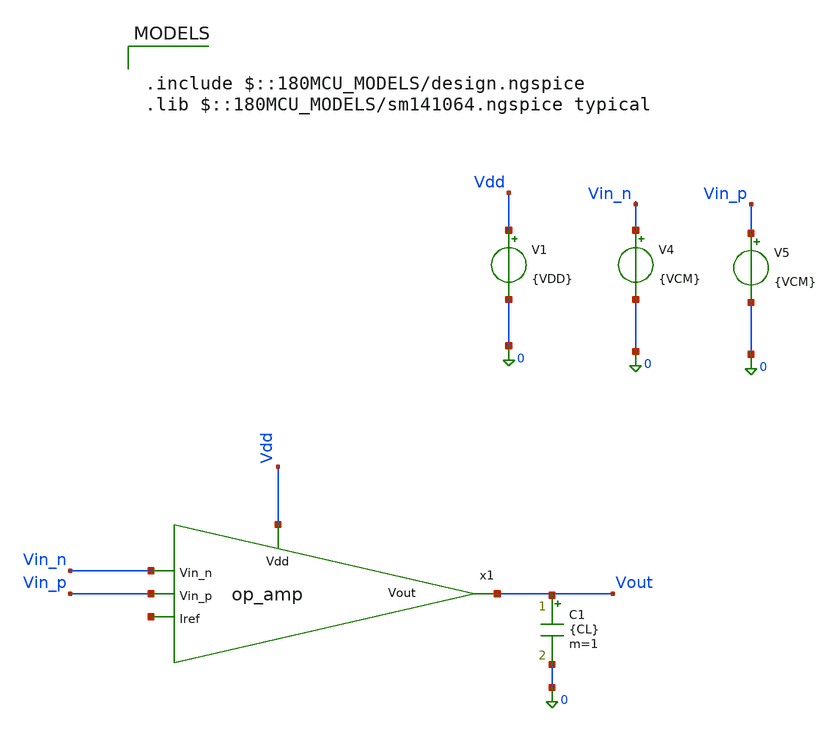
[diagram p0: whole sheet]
** sch_path: blocks/adc/lvds/ota_test.sch
**.subckt ota_test
C1 net1 0 {CL} m=1
V1 Vdd 0 {VDD}
V4 Vin_n 0 {VCM}
V5 Vin_p 0 {VCM}
x1 Vdd Vout Vin_n Vin_p net2 op_amp
**** begin user architecture code


.param VDD=3.3
.param VCM=1.2
.param VB1=0
.param VB2=0
.param CL=10f

.control
* ============================================================
* Output file
* ============================================================
let vb1_start = 0
let vb1_step  = 0.1
let vb1_n     = 33

let vb2_start = 0
let vb2_step  = 0.1
let vb2_n     = 33


shell rm /foss/designs/trans_testing/ota_testing/ota_bias_op_loop.txt

set appendwrite
set wr_singlescale

* ============================================================
* Main VB1 / VB2 operating-point loop
* ============================================================


  let i = 0

  while i le vb1_n

    let vb1_val = vb1_start + i*vb1_step
    let j = 0

    echo Starting VB1 = $&vb1_val

    while j le vb2_n

      let vb2_val = vb2_start + j*vb2_step

      alter V2 = $&vb1_val
      alter V3 = $&vb2_val

      op

      let vb1_save = vb1_val
      let vb2_save = vb2_val
      let vout_save = v(vout)

      let xm1_type  = 1
      let xm1_id    = @m.x1.xm1.m0[id]
      let xm1_vgs   = @m.x1.xm1.m0[vgs]
      let xm1_vds   = @m.x1.xm1.m0[vds]
      let xm1_vth   = @m.x1.xm1.m0[vth]
      let xm1_vdsat = @m.x1.xm1.m0[vdsat]
      let xm1_gm    = @m.x1.xm1.m0[gm]
      let xm1_gds   = @m.x1.xm1.m0[gds]

      let xm2_type  = 1
      let xm2_id    = @m.x1.xm2.m0[id]
      let xm2_vgs   = @m.x1.xm2.m0[vgs]
      let xm2_vds   = @m.x1.xm2.m0[vds]
      let xm2_vth   = @m.x1.xm2.m0[vth]
      let xm2_vdsat = @m.x1.xm2.m0[vdsat]
      let xm2_gm    = @m.x1.xm2.m0[gm]
      let xm2_gds   = @m.x1.xm2.m0[gds]

      let xm3_type  = 1
      let xm3_id    = @m.x1.xm3.m0[id]
      let xm3_vgs   = @m.x1.xm3.m0[vgs]
      let xm3_vds   = @m.x1.xm3.m0[vds]
      let xm3_vth   = @m.x1.xm3.m0[vth]
      let xm3_vdsat = @m.x1.xm3.m0[vdsat]
      let xm3_gm    = @m.x1.xm3.m0[gm]
      let xm3_gds   = @m.x1.xm3.m0[gds]

      let xm4_type  = 1
      let xm4_id    = @m.x1.xm4.m0[id]
      let xm4_vgs   = @m.x1.xm4.m0[vgs]
      let xm4_vds   = @m.x1.xm4.m0[vds]
      let xm4_vth   = @m.x1.xm4.m0[vth]
      let xm4_vdsat = @m.x1.xm4.m0[vdsat]
      let xm4_gm    = @m.x1.xm4.m0[gm]
      let xm4_gds   = @m.x1.xm4.m0[gds]

      let xm5_type  = 0
      let xm5_id    = @m.x1.xm5.m0[id]
      let xm5_vgs   = @m.x1.xm5.m0[vgs]
      let xm5_vds   = @m.x1.xm5.m0[vds]
      let xm5_vth   = @m.x1.xm5.m0[vth]
      let xm5_vdsat = @m.x1.xm5.m0[vdsat]
      let xm5_gm    = @m.x1.xm5.m0[gm]
      let xm5_gds   = @m.x1.xm5.m0[gds]

      let xm6_type  = 0
      let xm6_id    = @m.x1.xm6.m0[id]
      let xm6_vgs   = @m.x1.xm6.m0[vgs]
      let xm6_vds   = @m.x1.xm6.m0[vds]
      let xm6_vth   = @m.x1.xm6.m0[vth]
      let xm6_vdsat = @m.x1.xm6.m0[vdsat]
      let xm6_gm    = @m.x1.xm6.m0[gm]
      let xm6_gds   = @m.x1.xm6.m0[gds]

      let xm7_type  = 1
      let xm7_id    = @m.x1.xm7.m0[id]
      let xm7_vgs   = @m.x1.xm7.m0[vgs]
      let xm7_vds   = @m.x1.xm7.m0[vds]
      let xm7_vth   = @m.x1.xm7.m0[vth]
      let xm7_vdsat = @m.x1.xm7.m0[vdsat]
      let xm7_gm    = @m.x1.xm7.m0[gm]
      let xm7_gds   = @m.x1.xm7.m0[gds]

      let xm8_type  = 1
      let xm8_id    = @m.x1.xm8.m0[id]
      let xm8_vgs   = @m.x1.xm8.m0[vgs]
      let xm8_vds   = @m.x1.xm8.m0[vds]
      let xm8_vth   = @m.x1.xm8.m0[vth]
      let xm8_vdsat = @m.x1.xm8.m0[vdsat]
      let xm8_gm    = @m.x1.xm8.m0[gm]
      let xm8_gds   = @m.x1.xm8.m0[gds]

      let xm9_type  = 1
      let xm9_id    = @m.x1.xm9.m0[id]
      let xm9_vgs   = @m.x1.xm9.m0[vgs]
      let xm9_vds   = @m.x1.xm9.m0[vds]
      let xm9_vth   = @m.x1.xm9.m0[vth]
      let xm9_vdsat = @m.x1.xm9.m0[vdsat]
      let xm9_gm    = @m.x1.xm9.m0[gm]
      let xm9_gds   = @m.x1.xm9.m0[gds]

      let xm10_type  = 1
      let xm10_id    = @m.x1.xm10.m0[id]
      let xm10_vgs   = @m.x1.xm10.m0[vgs]
      let xm10_vds   = @m.x1.xm10.m0[vds]
      let xm10_vth   = @m.x1.xm10.m0[vth]
      let xm10_vdsat = @m.x1.xm10.m0[vdsat]
      let xm10_gm    = @m.x1.xm10.m0[gm]
      let xm10_gds   = @m.x1.xm10.m0[gds]

      let xm11_type  = 0
      let xm11_id    = @m.x1.xm11.m0[id]
      let xm11_vgs   = @m.x1.xm11.m0[vgs]
      let xm11_vds   = @m.x1.xm11.m0[vds]
      let xm11_vth   = @m.x1.xm11.m0[vth]
      let xm11_vdsat = @m.x1.xm11.m0[vdsat]
      let xm11_gm    = @m.x1.xm11.m0[gm]
      let xm11_gds   = @m.x1.xm11.m0[gds]

      let xm12_type  = 0
      let xm12_id    = @m.x1.xm12.m0[id]
      let xm12_vgs   = @m.x1.xm12.m0[vgs]
      let xm12_vds   = @m.x1.xm12.m0[vds]
      let xm12_vth   = @m.x1.xm12.m0[vth]
      let xm12_vdsat = @m.x1.xm12.m0[vdsat]
      let xm12_gm    = @m.x1.xm12.m0[gm]
      let xm12_gds   = @m.x1.xm12.m0[gds]

      let xm13_type  = 0
      let xm13_id    = @m.x1.xm13.m0[id]
      let xm13_vgs   = @m.x1.xm13.m0[vgs]
      let xm13_vds   = @m.x1.xm13.m0[vds]
      let xm13_vth   = @m.x1.xm13.m0[vth]
      let xm13_vdsat = @m.x1.xm13.m0[vdsat]
      let xm13_gm    = @m.x1.xm13.m0[gm]
      let xm13_gds   = @m.x1.xm13.m0[gds]

      let xm14_type  = 0
      let xm14_id    = @m.x1.xm14.m0[id]
      let xm14_vgs   = @m.x1.xm14.m0[vgs]
      let xm14_vds   = @m.x1.xm14.m0[vds]
      let xm14_vth   = @m.x1.xm14.m0[vth]
      let xm14_vdsat = @m.x1.xm14.m0[vdsat]
      let xm14_gm    = @m.x1.xm14.m0[gm]
      let xm14_gds   = @m.x1.xm14.m0[gds]

	wrdata /foss/designs/trans_testing/ota_testing/ota_bias_op_loop.txt vb1_save vb2_save vout_save
+ xm1_type xm1_id xm1_vgs xm1_vds xm1_vth xm1_vdsat xm1_gm xm1_gds xm2_type xm2_id xm2_vgs xm2_vds xm2_vth
+ xm2_vdsat xm2_gm xm2_gds xm3_type xm3_id xm3_vgs xm3_vds xm3_vth xm3_vdsat xm3_gm xm3_gds xm4_type xm4_id
+ xm4_vgs xm4_vds xm4_vth xm4_vdsat xm4_gm xm4_gds xm5_type xm5_id xm5_vgs xm5_vds xm5_vth xm5_vdsat xm5_gm
+ xm5_gds xm6_type xm6_id xm6_vgs xm6_vds xm6_vth xm6_vdsat xm6_gm xm6_gds xm7_type xm7_id xm7_vgs xm7_vds
+ xm7_vth xm7_vdsat xm7_gm xm7_gds xm8_type xm8_id xm8_vgs xm8_vds xm8_vth xm8_vdsat xm8_gm xm8_gds xm9_type
+ xm9_id xm9_vgs xm9_vds xm9_vth xm9_vdsat xm9_gm xm9_gds xm10_type xm10_id xm10_vgs xm10_vds xm10_vth
+ xm10_vdsat xm10_gm xm10_gds xm11_type xm11_id xm11_vgs xm11_vds xm11_vth xm11_vdsat xm11_gm xm11_gds xm12_type
+ xm12_id xm12_vgs xm12_vds xm12_vth xm12_vdsat xm12_gm xm12_gds xm13_type xm13_id xm13_vgs xm13_vds xm13_vth
+ xm13_vdsat xm13_gm xm13_gds xm14_type xm14_id xm14_vgs xm14_vds xm14_vth xm14_vdsat xm14_gm xm14_gds
      let j = j + 1

    end

    let i = i + 1

  end


.endc



.include $::180MCU_MODELS/design.ngspice
.lib $::180MCU_MODELS/sm141064.ngspice typical

**** end user architecture code
**.ends

* expanding   symbol:  op_amp.sym # of pins=5
** sym_path: blocks/adc/lvds/op_amp.sym
** sch_path: blocks/adc/lvds/op_amp.sch
.subckt op_amp Vdd Vout Vin_n Vin_p Iref
*.ipin Vdd
*.ipin Vin_p
*.ipin Vin_n
*.opin Vout
*.ipin Iref
XM1 net2 net3 Vdd Vdd pfet_03v3 L=0.28u W=10.5u nf=1 ad='int((nf+1)/2) * W/nf * 0.18u' as='int((nf+2)/2) * W/nf * 0.18u'
+ pd='2*int((nf+1)/2) * (W/nf + 0.18u)' ps='2*int((nf+2)/2) * (W/nf + 0.18u)' nrd='0.18u / W' nrs='0.18u / W'
+ sa=0 sb=0 sd=0 m=1
XM2 net1 net4 Vdd Vdd pfet_03v3 L=0.28u W=10.5u nf=1 ad='int((nf+1)/2) * W/nf * 0.18u' as='int((nf+2)/2) * W/nf * 0.18u'
+ pd='2*int((nf+1)/2) * (W/nf + 0.18u)' ps='2*int((nf+2)/2) * (W/nf + 0.18u)' nrd='0.18u / W' nrs='0.18u / W'
+ sa=0 sb=0 sd=0 m=1
XM3 net3 Vb2 net2 Vdd pfet_03v3 L=0.28u W=10.5u nf=1 ad='int((nf+1)/2) * W/nf * 0.18u' as='int((nf+2)/2) * W/nf * 0.18u'
+ pd='2*int((nf+1)/2) * (W/nf + 0.18u)' ps='2*int((nf+2)/2) * (W/nf + 0.18u)' nrd='0.18u / W' nrs='0.18u / W'
+ sa=0 sb=0 sd=0 m=1
XM4 net4 Vb2 net1 Vdd pfet_03v3 L=0.28u W=10.5u nf=1 ad='int((nf+1)/2) * W/nf * 0.18u' as='int((nf+2)/2) * W/nf * 0.18u'
+ pd='2*int((nf+1)/2) * (W/nf + 0.18u)' ps='2*int((nf+2)/2) * (W/nf + 0.18u)' nrd='0.18u / W' nrs='0.18u / W'
+ sa=0 sb=0 sd=0 m=1
XM5 net4 Vin_p net5 0 nfet_03v3 L=0.28u W=52.5u nf=15 ad='int((nf+1)/2) * W/nf * 0.18u' as='int((nf+2)/2) * W/nf * 0.18u'
+ pd='2*int((nf+1)/2) * (W/nf + 0.18u)' ps='2*int((nf+2)/2) * (W/nf + 0.18u)' nrd='0.18u / W' nrs='0.18u / W'
+ sa=0 sb=0 sd=0 m=1
XM6 net3 Vin_n net5 0 nfet_03v3 L=0.28u W=52.5u nf=15 ad='int((nf+1)/2) * W/nf * 0.18u' as='int((nf+2)/2) * W/nf * 0.18u'
+ pd='2*int((nf+1)/2) * (W/nf + 0.18u)' ps='2*int((nf+2)/2) * (W/nf + 0.18u)' nrd='0.18u / W' nrs='0.18u / W'
+ sa=0 sb=0 sd=0 m=1
XM7 net6 net4 Vdd Vdd pfet_03v3 L=0.28u W=10.5u nf=1 ad='int((nf+1)/2) * W/nf * 0.18u' as='int((nf+2)/2) * W/nf * 0.18u'
+ pd='2*int((nf+1)/2) * (W/nf + 0.18u)' ps='2*int((nf+2)/2) * (W/nf + 0.18u)' nrd='0.18u / W' nrs='0.18u / W'
+ sa=0 sb=0 sd=0 m=1
XM9 net7 net3 Vdd Vdd pfet_03v3 L=0.28u W=10.5u nf=1 ad='int((nf+1)/2) * W/nf * 0.18u' as='int((nf+2)/2) * W/nf * 0.18u'
+ pd='2*int((nf+1)/2) * (W/nf + 0.18u)' ps='2*int((nf+2)/2) * (W/nf + 0.18u)' nrd='0.18u / W' nrs='0.18u / W'
+ sa=0 sb=0 sd=0 m=1
XM11 net8 Vb2 net10 0 nfet_03v3 L=0.28u W=5.25u nf=1 ad='int((nf+1)/2) * W/nf * 0.18u' as='int((nf+2)/2) * W/nf * 0.18u'
+ pd='2*int((nf+1)/2) * (W/nf + 0.18u)' ps='2*int((nf+2)/2) * (W/nf + 0.18u)' nrd='0.18u / W' nrs='0.18u / W'
+ sa=0 sb=0 sd=0 m=1
XM12 Vout Vb2 net9 0 nfet_03v3 L=0.28u W=5.25u nf=1 ad='int((nf+1)/2) * W/nf * 0.18u' as='int((nf+2)/2) * W/nf * 0.18u'
+ pd='2*int((nf+1)/2) * (W/nf + 0.18u)' ps='2*int((nf+2)/2) * (W/nf + 0.18u)' nrd='0.18u / W' nrs='0.18u / W'
+ sa=0 sb=0 sd=0 m=1
XM13 net10 net8 0 0 nfet_03v3 L=0.28u W=5.25u nf=1 ad='int((nf+1)/2) * W/nf * 0.18u' as='int((nf+2)/2) * W/nf * 0.18u'
+ pd='2*int((nf+1)/2) * (W/nf + 0.18u)' ps='2*int((nf+2)/2) * (W/nf + 0.18u)' nrd='0.18u / W' nrs='0.18u / W'
+ sa=0 sb=0 sd=0 m=1
XM14 net9 net8 0 0 nfet_03v3 L=0.28u W=5.25u nf=1 ad='int((nf+1)/2) * W/nf * 0.18u' as='int((nf+2)/2) * W/nf * 0.18u'
+ pd='2*int((nf+1)/2) * (W/nf + 0.18u)' ps='2*int((nf+2)/2) * (W/nf + 0.18u)' nrd='0.18u / W' nrs='0.18u / W'
+ sa=0 sb=0 sd=0 m=1
XM8 net8 0 net6 Vdd pfet_03v3 L=0.28u W=10.5u nf=1 ad='int((nf+1)/2) * W/nf * 0.18u' as='int((nf+2)/2) * W/nf * 0.18u'
+ pd='2*int((nf+1)/2) * (W/nf + 0.18u)' ps='2*int((nf+2)/2) * (W/nf + 0.18u)' nrd='0.18u / W' nrs='0.18u / W'
+ sa=0 sb=0 sd=0 m=1
XM10 Vout 0 net7 Vdd pfet_03v3 L=0.28u W=10.5u nf=1 ad='int((nf+1)/2) * W/nf * 0.18u' as='int((nf+2)/2) * W/nf * 0.18u'
+ pd='2*int((nf+1)/2) * (W/nf + 0.18u)' ps='2*int((nf+2)/2) * (W/nf + 0.18u)' nrd='0.18u / W' nrs='0.18u / W'
+ sa=0 sb=0 sd=0 m=1
XM15 net5 net11 0 0 nfet_03v3 L=1u W=80u nf=20 ad='int((nf+1)/2) * W/nf * 0.18u' as='int((nf+2)/2) * W/nf * 0.18u'
+ pd='2*int((nf+1)/2) * (W/nf + 0.18u)' ps='2*int((nf+2)/2) * (W/nf + 0.18u)' nrd='0.18u / W' nrs='0.18u / W'
+ sa=0 sb=0 sd=0 m=1
XM16 Iref Iref Vdd Vdd pfet_03v3 L=1u W=20u nf=1 ad='int((nf+1)/2) * W/nf * 0.18u' as='int((nf+2)/2) * W/nf * 0.18u'
+ pd='2*int((nf+1)/2) * (W/nf + 0.18u)' ps='2*int((nf+2)/2) * (W/nf + 0.18u)' nrd='0.18u / W' nrs='0.18u / W'
+ sa=0 sb=0 sd=0 m=1
XM17 net11 Iref Vdd Vdd pfet_03v3 L=1u W=80u nf=1 ad='int((nf+1)/2) * W/nf * 0.18u' as='int((nf+2)/2) * W/nf * 0.18u'
+ pd='2*int((nf+1)/2) * (W/nf + 0.18u)' ps='2*int((nf+2)/2) * (W/nf + 0.18u)' nrd='0.18u / W' nrs='0.18u / W'
+ sa=0 sb=0 sd=0 m=1
XM18 Vb2 Iref Vdd Vdd pfet_03v3 L=1u W=20u nf=1 ad='int((nf+1)/2) * W/nf * 0.18u' as='int((nf+2)/2) * W/nf * 0.18u'
+ pd='2*int((nf+1)/2) * (W/nf + 0.18u)' ps='2*int((nf+2)/2) * (W/nf + 0.18u)' nrd='0.18u / W' nrs='0.18u / W'
+ sa=0 sb=0 sd=0 m=1
XM19 Vb2 Vb2 net12 0 nfet_03v3 L=0.28u W=30u nf=1 ad='int((nf+1)/2) * W/nf * 0.18u' as='int((nf+2)/2) * W/nf * 0.18u'
+ pd='2*int((nf+1)/2) * (W/nf + 0.18u)' ps='2*int((nf+2)/2) * (W/nf + 0.18u)' nrd='0.18u / W' nrs='0.18u / W'
+ sa=0 sb=0 sd=0 m=1
XM20 net12 net12 0 0 nfet_03v3 L=0.28u W=30u nf=1 ad='int((nf+1)/2) * W/nf * 0.18u' as='int((nf+2)/2) * W/nf * 0.18u'
+ pd='2*int((nf+1)/2) * (W/nf + 0.18u)' ps='2*int((nf+2)/2) * (W/nf + 0.18u)' nrd='0.18u / W' nrs='0.18u / W'
+ sa=0 sb=0 sd=0 m=1
XM21 net11 net11 0 0 nfet_03v3 L=1u W=80u nf=1 ad='int((nf+1)/2) * W/nf * 0.18u' as='int((nf+2)/2) * W/nf * 0.18u'
+ pd='2*int((nf+1)/2) * (W/nf + 0.18u)' ps='2*int((nf+2)/2) * (W/nf + 0.18u)' nrd='0.18u / W' nrs='0.18u / W'
+ sa=0 sb=0 sd=0 m=1
.ends

.end
